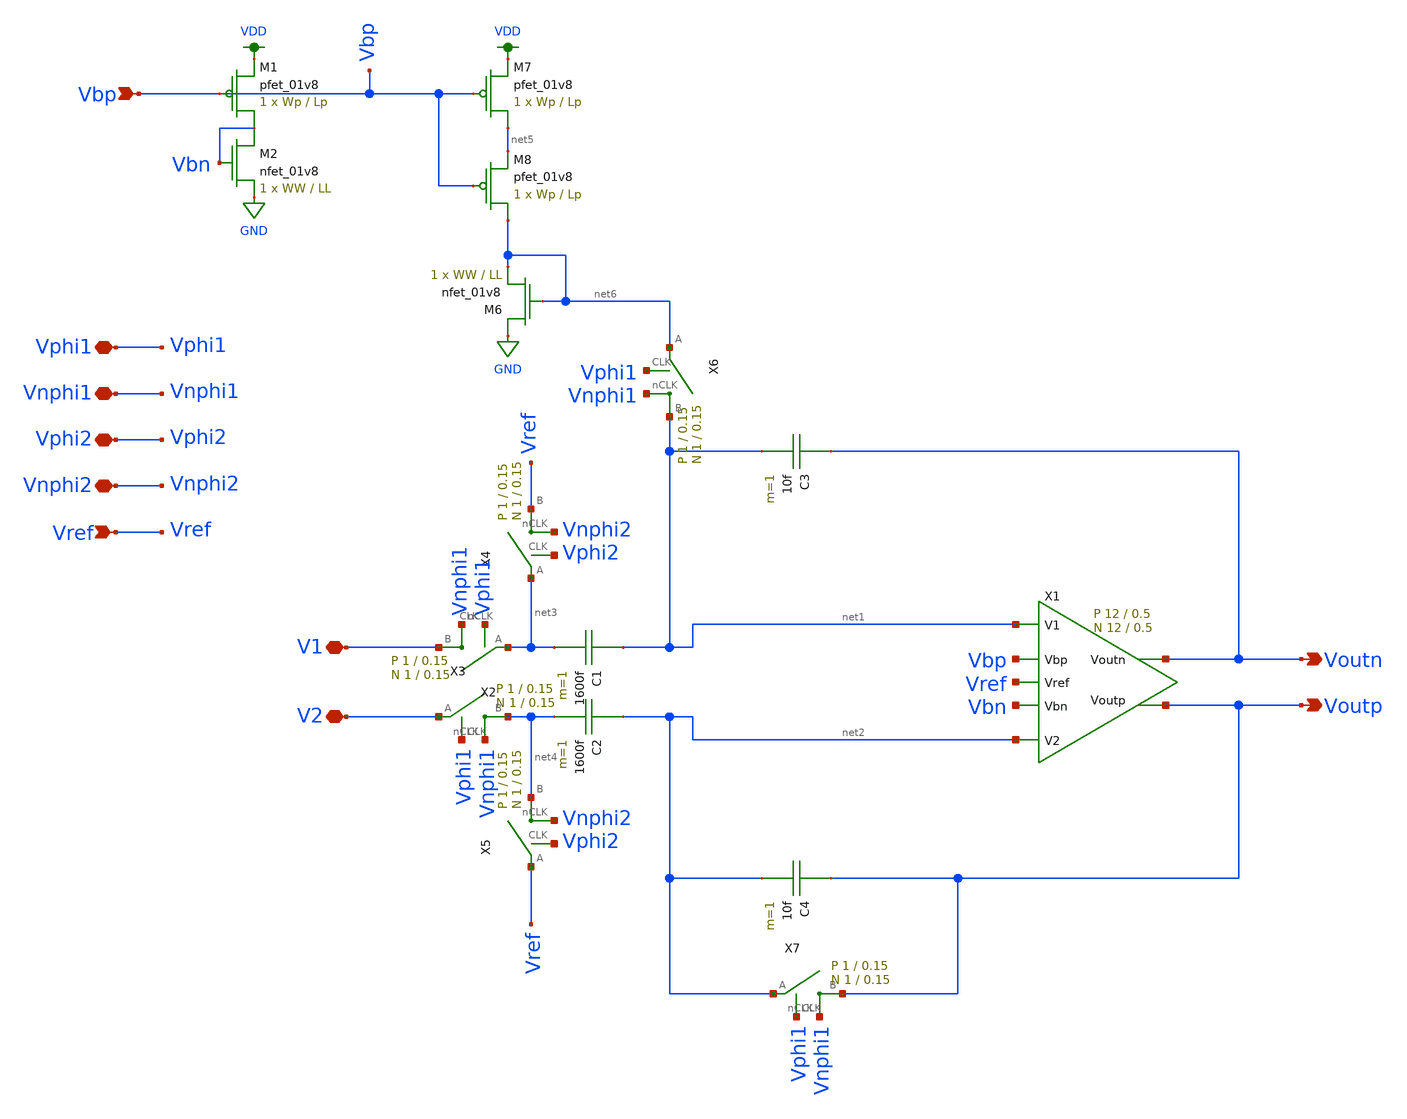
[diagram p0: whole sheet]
** sch_path: schematic/FD_diffamp_160.sch
**.subckt FD_diffamp_160 Vbp Vphi1 Vnphi1 Vphi2 Vnphi2 V1 V2 Voutn Voutp Vref
*.ipin Vbp
*.iopin Vphi1
*.iopin Vnphi1
*.iopin Vphi2
*.iopin Vnphi2
*.iopin V1
*.iopin V2
*.opin Voutn
*.opin Voutp
*.ipin Vref
X1 net1 net2 Voutp Voutn Vbp Vref Vbn fully_differential_sc_amp Wp=12 Lp=0.5 WW=12 LL=0.5
C1 net1 net3 1600f m=1
C2 net2 net4 1600f m=1
C3 Voutn net1 10f m=1
C4 Voutp net2 10f m=1
X2 V1 net3 Vphi1 Vnphi1 switch Wp=1 Lp=0.15 WW=1 LL=0.15
X3 net4 V2 Vphi1 Vnphi1 switch Wp=1 Lp=0.15 WW=1 LL=0.15
X4 Vref net3 Vphi2 Vnphi2 switch Wp=1 Lp=0.15 WW=1 LL=0.15
X5 net4 Vref Vphi2 Vnphi2 switch Wp=1 Lp=0.15 WW=1 LL=0.15
X6 net1 net6 Vphi1 Vnphi1 switch Wp=1 Lp=0.15 WW=1 LL=0.15
X7 Voutp net2 Vphi1 Vnphi1 switch Wp=1 Lp=0.15 WW=1 LL=0.15
XM7 net5 Vbp VDD VDD sky130_fd_pr__pfet_01v8 L=Lp W=Wp nf=1 ad='int((nf+1)/2) * W/nf * 0.29' as='int((nf+2)/2) * W/nf * 0.29'
+ pd='2*int((nf+1)/2) * (W/nf + 0.29)' ps='2*int((nf+2)/2) * (W/nf + 0.29)' nrd='0.29 / W' nrs='0.29 / W'
+ sa=0 sb=0 sd=0 mult=1 m=1
XM8 net6 Vbp net5 VDD sky130_fd_pr__pfet_01v8 L=Lp W=Wp nf=1 ad='int((nf+1)/2) * W/nf * 0.29' as='int((nf+2)/2) * W/nf * 0.29'
+ pd='2*int((nf+1)/2) * (W/nf + 0.29)' ps='2*int((nf+2)/2) * (W/nf + 0.29)' nrd='0.29 / W' nrs='0.29 / W'
+ sa=0 sb=0 sd=0 mult=1 m=1
XM6 GND net6 net6 GND sky130_fd_pr__nfet_01v8 L=LL W=WW nf=1 ad='int((nf+1)/2) * W/nf * 0.29' as='int((nf+2)/2) * W/nf * 0.29'
+ pd='2*int((nf+1)/2) * (W/nf + 0.29)' ps='2*int((nf+2)/2) * (W/nf + 0.29)' nrd='0.29 / W' nrs='0.29 / W'
+ sa=0 sb=0 sd=0 mult=1 m=1
XM1 Vbn Vbp VDD VDD sky130_fd_pr__pfet_01v8 L=Lp W=Wp nf=1 ad='int((nf+1)/2) * W/nf * 0.29' as='int((nf+2)/2) * W/nf * 0.29'
+ pd='2*int((nf+1)/2) * (W/nf + 0.29)' ps='2*int((nf+2)/2) * (W/nf + 0.29)' nrd='0.29 / W' nrs='0.29 / W'
+ sa=0 sb=0 sd=0 mult=1 m=1
XM2 Vbn Vbn GND GND sky130_fd_pr__nfet_01v8 L=LL W=WW nf=1 ad='int((nf+1)/2) * W/nf * 0.29' as='int((nf+2)/2) * W/nf * 0.29'
+ pd='2*int((nf+1)/2) * (W/nf + 0.29)' ps='2*int((nf+2)/2) * (W/nf + 0.29)' nrd='0.29 / W' nrs='0.29 / W'
+ sa=0 sb=0 sd=0 mult=1 m=1
**.ends

* expanding   symbol:
*+  /home/madvlsi/Documents/MADVLSI-Final_Project/schematic/fully_differential_sc_amp.sym # of pins=7
** sym_path: schematic/archive/fully_differential_sc_amp.sym
** sch_path: schematic/archive/fully_differential_sc_amp.sch
.subckt fully_differential_sc_amp V1 V2 Voutp Voutn Vbp Vref Vbn  Wp=1 Lp=0.15 WW=1 LL=0.15
*.ipin V1
*.ipin V2
*.ipin Vbp
*.ipin Vbn
*.ipin Vref
*.iopin Voutp
*.iopin Voutn
XM1a net2 V1 GND GND sky130_fd_pr__nfet_01v8 L=LL W=WW nf=1 ad='int((nf+1)/2) * W/nf * 0.29' as='int((nf+2)/2) * W/nf * 0.29'
+ pd='2*int((nf+1)/2) * (W/nf + 0.29)' ps='2*int((nf+2)/2) * (W/nf + 0.29)' nrd='0.29 / W' nrs='0.29 / W'
+ sa=0 sb=0 sd=0 mult=1 m=1
XM1b Voutn V1 GND GND sky130_fd_pr__nfet_01v8 L=LL W=WW nf=1 ad='int((nf+1)/2) * W/nf * 0.29' as='int((nf+2)/2) * W/nf * 0.29'
+ pd='2*int((nf+1)/2) * (W/nf + 0.29)' ps='2*int((nf+2)/2) * (W/nf + 0.29)' nrd='0.29 / W' nrs='0.29 / W'
+ sa=0 sb=0 sd=0 mult=1 m=1
XM2b Voutp V2 GND GND sky130_fd_pr__nfet_01v8 L=LL W=WW nf=1 ad='int((nf+1)/2) * W/nf * 0.29' as='int((nf+2)/2) * W/nf * 0.29'
+ pd='2*int((nf+1)/2) * (W/nf + 0.29)' ps='2*int((nf+2)/2) * (W/nf + 0.29)' nrd='0.29 / W' nrs='0.29 / W'
+ sa=0 sb=0 sd=0 mult=1 m=1
XM2a net2 V2 GND GND sky130_fd_pr__nfet_01v8 L=LL W=WW nf=1 ad='int((nf+1)/2) * W/nf * 0.29' as='int((nf+2)/2) * W/nf * 0.29'
+ pd='2*int((nf+1)/2) * (W/nf + 0.29)' ps='2*int((nf+2)/2) * (W/nf + 0.29)' nrd='0.29 / W' nrs='0.29 / W'
+ sa=0 sb=0 sd=0 mult=1 m=1
XMb net2 Vbp VDD VDD sky130_fd_pr__pfet_01v8 L=Lp W=Wp nf=1 ad='int((nf+1)/2) * W/nf * 0.29' as='int((nf+2)/2) * W/nf * 0.29'
+ pd='2*int((nf+1)/2) * (W/nf + 0.29)' ps='2*int((nf+2)/2) * (W/nf + 0.29)' nrd='0.29 / W' nrs='0.29 / W'
+ sa=0 sb=0 sd=0 mult=1 m=1
C2b net2 V2 1600f m=1
C2a net2 V1 1600f m=1
XM1 GND V2 net1 GND sky130_fd_pr__nfet_01v8 L=LL W=WW nf=1 ad='int((nf+1)/2) * W/nf * 0.29' as='int((nf+2)/2) * W/nf * 0.29'
+ pd='2*int((nf+1)/2) * (W/nf + 0.29)' ps='2*int((nf+2)/2) * (W/nf + 0.29)' nrd='0.29 / W' nrs='0.29 / W'
+ sa=0 sb=0 sd=0 mult=1 m=1
XM2 GND V1 net1 GND sky130_fd_pr__nfet_01v8 L=LL W=WW nf=1 ad='int((nf+1)/2) * W/nf * 0.29' as='int((nf+2)/2) * W/nf * 0.29'
+ pd='2*int((nf+1)/2) * (W/nf + 0.29)' ps='2*int((nf+2)/2) * (W/nf + 0.29)' nrd='0.29 / W' nrs='0.29 / W'
+ sa=0 sb=0 sd=0 mult=1 m=1
XMb1 VDD net4 net5 VDD sky130_fd_pr__pfet_01v8 L=Lp W=Wp nf=1 ad='int((nf+1)/2) * W/nf * 0.29' as='int((nf+2)/2) * W/nf * 0.29'
+ pd='2*int((nf+1)/2) * (W/nf + 0.29)' ps='2*int((nf+2)/2) * (W/nf + 0.29)' nrd='0.29 / W' nrs='0.29 / W'
+ sa=0 sb=0 sd=0 mult=1 m=1
XMb2 VDD net4 net1 VDD sky130_fd_pr__pfet_01v8 L=Lp W=Wp nf=1 ad='int((nf+1)/2) * W/nf * 0.29' as='int((nf+2)/2) * W/nf * 0.29'
+ pd='2*int((nf+1)/2) * (W/nf + 0.29)' ps='2*int((nf+2)/2) * (W/nf + 0.29)' nrd='0.29 / W' nrs='0.29 / W'
+ sa=0 sb=0 sd=0 mult=1 m=1
XMb4 VDD net4 net6 VDD sky130_fd_pr__pfet_01v8 L=Lp W=Wp nf=1 ad='int((nf+1)/2) * W/nf * 0.29' as='int((nf+2)/2) * W/nf * 0.29'
+ pd='2*int((nf+1)/2) * (W/nf + 0.29)' ps='2*int((nf+2)/2) * (W/nf + 0.29)' nrd='0.29 / W' nrs='0.29 / W'
+ sa=0 sb=0 sd=0 mult=1 m=1
XMb5 net7 net4 VDD VDD sky130_fd_pr__pfet_01v8 L=Lp W=Wp nf=1 ad='int((nf+1)/2) * W/nf * 0.29' as='int((nf+2)/2) * W/nf * 0.29'
+ pd='2*int((nf+1)/2) * (W/nf + 0.29)' ps='2*int((nf+2)/2) * (W/nf + 0.29)' nrd='0.29 / W' nrs='0.29 / W'
+ sa=0 sb=0 sd=0 mult=1 m=1
XM3 net3 Vbn GND GND sky130_fd_pr__nfet_01v8 L=LL W=WW nf=1 ad='int((nf+1)/2) * W/nf * 0.29' as='int((nf+2)/2) * W/nf * 0.29'
+ pd='2*int((nf+1)/2) * (W/nf + 0.29)' ps='2*int((nf+2)/2) * (W/nf + 0.29)' nrd='0.29 / W' nrs='0.29 / W'
+ sa=0 sb=0 sd=0 mult=1 m=1
XM4 VDD net1 net3 GND sky130_fd_pr__nfet_01v8 L=LL W=WW nf=1 ad='int((nf+1)/2) * W/nf * 0.29' as='int((nf+2)/2) * W/nf * 0.29'
+ pd='2*int((nf+1)/2) * (W/nf + 0.29)' ps='2*int((nf+2)/2) * (W/nf + 0.29)' nrd='0.29 / W' nrs='0.29 / W'
+ sa=0 sb=0 sd=0 mult=1 m=1
XM5 net3 Vref net4 GND sky130_fd_pr__nfet_01v8 L=LL W=WW nf=1 ad='int((nf+1)/2) * W/nf * 0.29' as='int((nf+2)/2) * W/nf * 0.29'
+ pd='2*int((nf+1)/2) * (W/nf + 0.29)' ps='2*int((nf+2)/2) * (W/nf + 0.29)' nrd='0.29 / W' nrs='0.29 / W'
+ sa=0 sb=0 sd=0 mult=1 m=1
XMb6 net5 net4 Voutn VDD sky130_fd_pr__pfet_01v8 L=Lp W=Wp nf=1 ad='int((nf+1)/2) * W/nf * 0.29' as='int((nf+2)/2) * W/nf * 0.29'
+ pd='2*int((nf+1)/2) * (W/nf + 0.29)' ps='2*int((nf+2)/2) * (W/nf + 0.29)' nrd='0.29 / W' nrs='0.29 / W'
+ sa=0 sb=0 sd=0 mult=1 m=1
XMb7 net6 net4 Voutp VDD sky130_fd_pr__pfet_01v8 L=Lp W=Wp nf=1 ad='int((nf+1)/2) * W/nf * 0.29' as='int((nf+2)/2) * W/nf * 0.29'
+ pd='2*int((nf+1)/2) * (W/nf + 0.29)' ps='2*int((nf+2)/2) * (W/nf + 0.29)' nrd='0.29 / W' nrs='0.29 / W'
+ sa=0 sb=0 sd=0 mult=1 m=1
XMb8 net4 net4 net7 VDD sky130_fd_pr__pfet_01v8 L=Lp W=Wp nf=1 ad='int((nf+1)/2) * W/nf * 0.29' as='int((nf+2)/2) * W/nf * 0.29'
+ pd='2*int((nf+1)/2) * (W/nf + 0.29)' ps='2*int((nf+2)/2) * (W/nf + 0.29)' nrd='0.29 / W' nrs='0.29 / W'
+ sa=0 sb=0 sd=0 mult=1 m=1
.ends


* expanding   symbol:  /home/madvlsi/Documents/MADVLSI-Final_Project/schematic/switch.sym # of
*+ pins=4
** sym_path: schematic/switch.sym
** sch_path: schematic/switch.sch
.subckt switch B A CLK nCLK  Wp=1 Lp=0.15 WW=1 LL=0.15
*.iopin B
*.iopin A
*.ipin CLK
*.ipin nCLK
*.ipin CLK
*.ipin CLK
*.ipin nCLK
*.ipin nCLK
XM1 A CLK B GND sky130_fd_pr__nfet_01v8 L={LL} W={WW} nf=1 ad='int((nf+1)/2) * W/nf * 0.29' as='int((nf+2)/2) * W/nf * 0.29'
+ pd='2*int((nf+1)/2) * (W/nf + 0.29)' ps='2*int((nf+2)/2) * (W/nf + 0.29)' nrd='0.29 / W' nrs='0.29 / W'
+ sa=0 sb=0 sd=0 mult=1 m=1
XM2 A nCLK B VDD sky130_fd_pr__pfet_01v8 L={Lp} W={Wp} nf=1 ad='int((nf+1)/2) * W/nf * 0.29' as='int((nf+2)/2) * W/nf * 0.29'
+ pd='2*int((nf+1)/2) * (W/nf + 0.29)' ps='2*int((nf+2)/2) * (W/nf + 0.29)' nrd='0.29 / W' nrs='0.29 / W'
+ sa=0 sb=0 sd=0 mult=1 m=1
XM3 B CLK B VDD sky130_fd_pr__pfet_01v8 L={Lp} W={Wp/2} nf=1 ad='int((nf+1)/2) * W/nf * 0.29' as='int((nf+2)/2) * W/nf * 0.29'
+ pd='2*int((nf+1)/2) * (W/nf + 0.29)' ps='2*int((nf+2)/2) * (W/nf + 0.29)' nrd='0.29 / W' nrs='0.29 / W'
+ sa=0 sb=0 sd=0 mult=1 m=1
XM4 A CLK A VDD sky130_fd_pr__pfet_01v8 L={Lp} W={Wp/2} nf=1 ad='int((nf+1)/2) * W/nf * 0.29' as='int((nf+2)/2) * W/nf * 0.29'
+ pd='2*int((nf+1)/2) * (W/nf + 0.29)' ps='2*int((nf+2)/2) * (W/nf + 0.29)' nrd='0.29 / W' nrs='0.29 / W'
+ sa=0 sb=0 sd=0 mult=1 m=1
XM5 B nCLK B GND sky130_fd_pr__nfet_01v8 L={LL} W={WW/2} nf=1 ad='int((nf+1)/2) * W/nf * 0.29' as='int((nf+2)/2) * W/nf * 0.29'
+ pd='2*int((nf+1)/2) * (W/nf + 0.29)' ps='2*int((nf+2)/2) * (W/nf + 0.29)' nrd='0.29 / W' nrs='0.29 / W'
+ sa=0 sb=0 sd=0 mult=1 m=1
XM6 A nCLK A GND sky130_fd_pr__nfet_01v8 L={LL} W={WW/2} nf=1 ad='int((nf+1)/2) * W/nf * 0.29' as='int((nf+2)/2) * W/nf * 0.29'
+ pd='2*int((nf+1)/2) * (W/nf + 0.29)' ps='2*int((nf+2)/2) * (W/nf + 0.29)' nrd='0.29 / W' nrs='0.29 / W'
+ sa=0 sb=0 sd=0 mult=1 m=1
.ends

.GLOBAL VDD
.GLOBAL GND
.end
